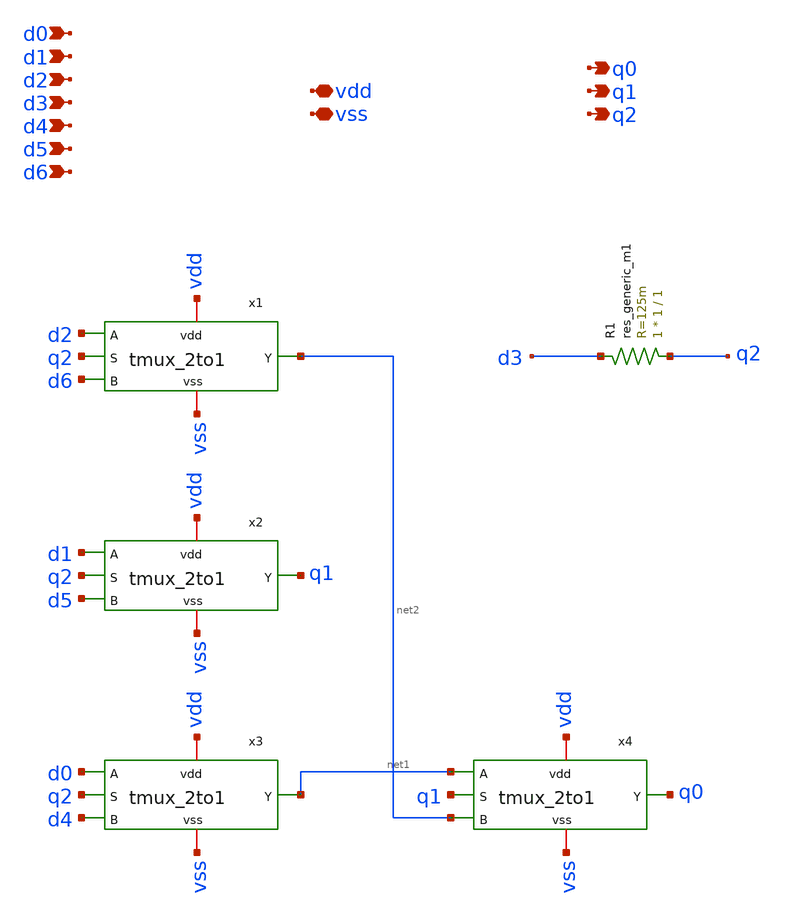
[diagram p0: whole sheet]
** sch_path: xsch/ip/tgates/tmux_7therm_to_3bin_.sch
**.subckt tmux_7therm_to_3bin_ d0 vdd q0 d1 d2 d3 d4 d5 d6 q1 q2 vss
*.ipin d0
*.iopin vdd
*.opin q0
*.ipin d1
*.ipin d2
*.ipin d3
*.ipin d4
*.ipin d5
*.ipin d6
*.opin q1
*.opin q2
*.iopin vss
x1 d2 vdd net2 q2 vss d6 tmux_2to1
x2 d1 vdd q1 q2 vss d5 tmux_2to1
x3 d0 vdd net1 q2 vss d4 tmux_2to1
x4 net1 vdd q0 q1 vss net2 tmux_2to1
R1 q2 d3 sky130_fd_pr__res_generic_m1 W=1 L=1 m=1
**.ends
.end
